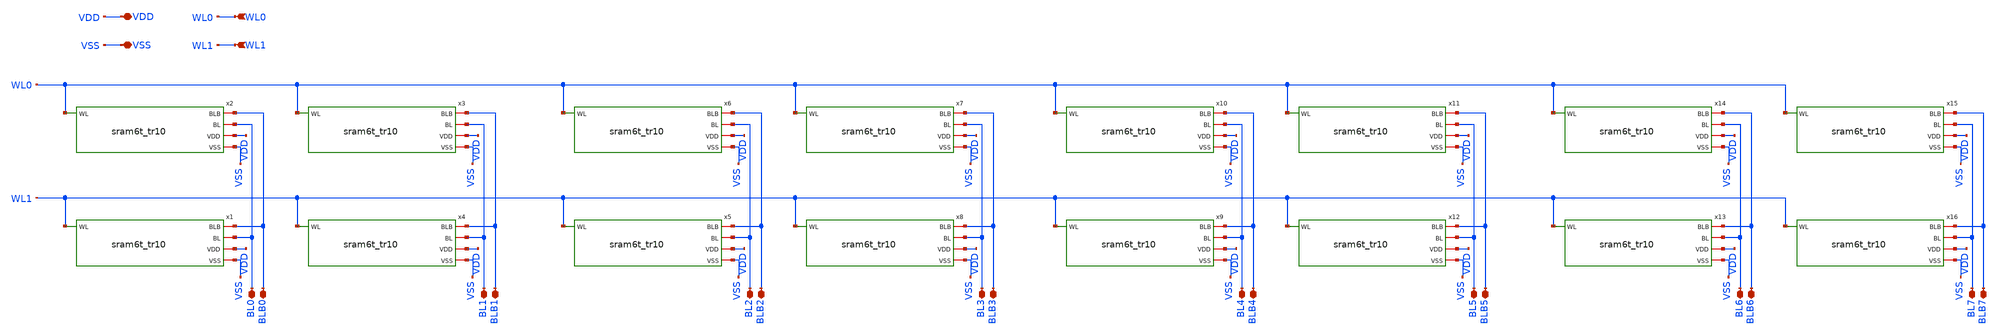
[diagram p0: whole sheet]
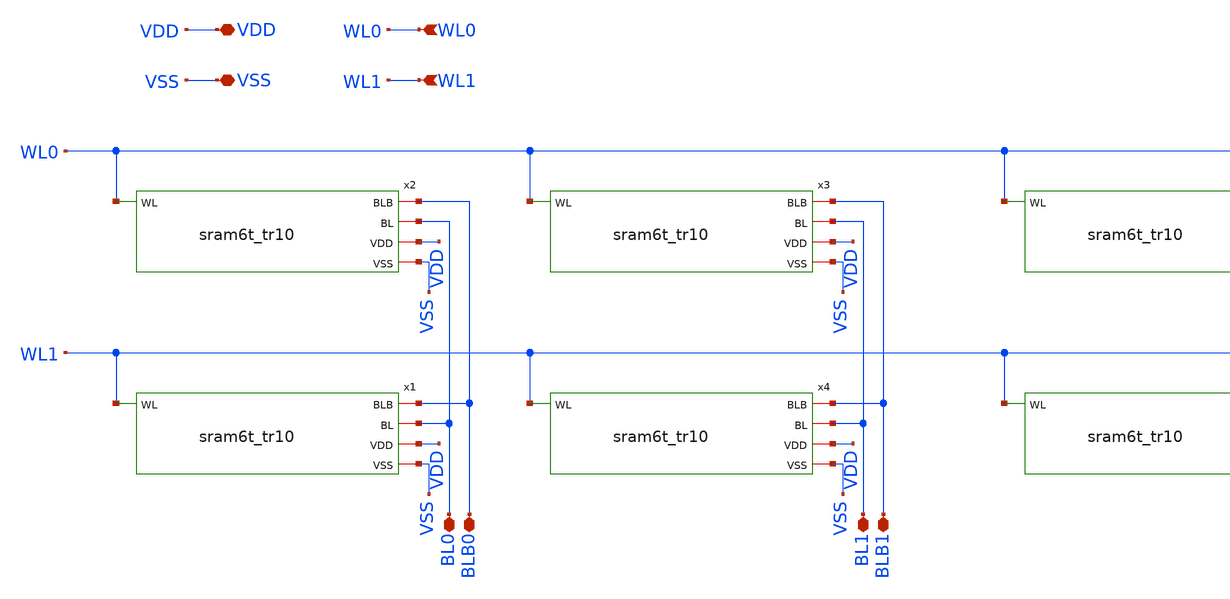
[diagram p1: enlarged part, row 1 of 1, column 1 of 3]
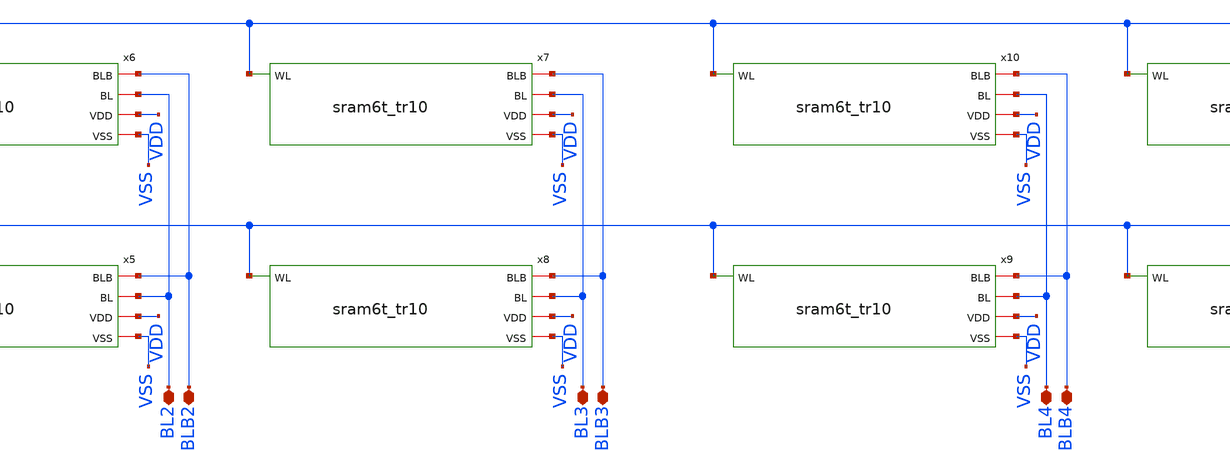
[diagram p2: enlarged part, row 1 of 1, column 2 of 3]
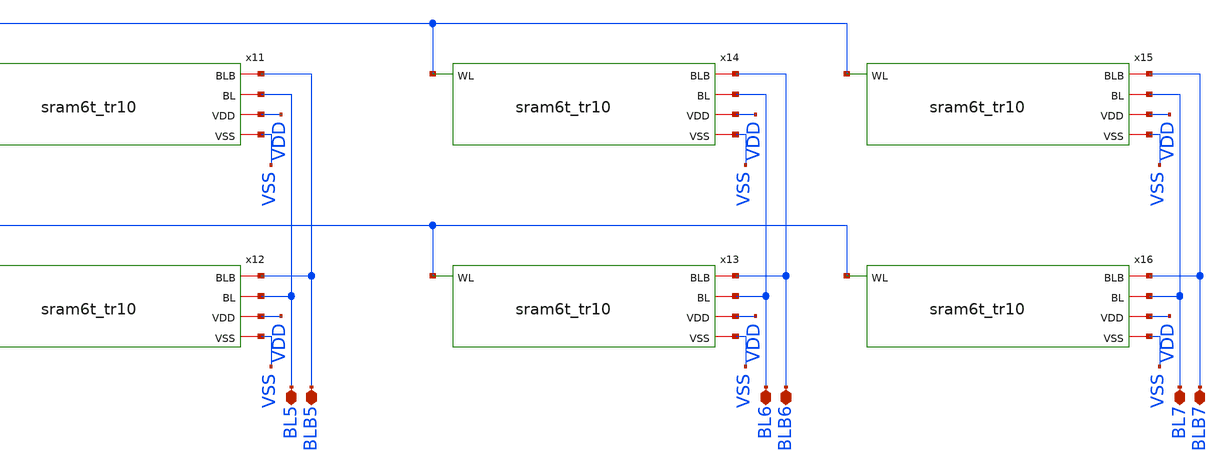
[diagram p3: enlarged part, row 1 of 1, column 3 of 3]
** sch_path: array/8word_x_2bit/sram_2w8b.sch
**.subckt sram_2w8b VDD VSS WL0 WL1 BL0 BLB0 BL1 BLB1 BL2 BLB2 BL3 BLB3 BL4 BLB4 BL5 BLB5 BL6 BLB6
*+ BL7 BLB7
*.iopin VDD
*.iopin VSS
*.ipin WL0
*.ipin WL1
*.iopin BL0
*.iopin BLB0
*.iopin BL1
*.iopin BLB1
*.iopin BL2
*.iopin BLB2
*.iopin BL3
*.iopin BLB3
*.iopin BL4
*.iopin BLB4
*.iopin BL5
*.iopin BLB5
*.iopin BL6
*.iopin BLB6
*.iopin BL7
*.iopin BLB7
x1 BL0 BLB0 WL1 VDD VSS sram6t_tr10
x2 BL0 BLB0 WL0 VDD VSS sram6t_tr10
x3 BL1 BLB1 WL0 VDD VSS sram6t_tr10
x4 BL1 BLB1 WL1 VDD VSS sram6t_tr10
x5 BL2 BLB2 WL1 VDD VSS sram6t_tr10
x6 BL2 BLB2 WL0 VDD VSS sram6t_tr10
x7 BL3 BLB3 WL0 VDD VSS sram6t_tr10
x8 BL3 BLB3 WL1 VDD VSS sram6t_tr10
x9 BL4 BLB4 WL1 VDD VSS sram6t_tr10
x10 BL4 BLB4 WL0 VDD VSS sram6t_tr10
x11 BL5 BLB5 WL0 VDD VSS sram6t_tr10
x12 BL5 BLB5 WL1 VDD VSS sram6t_tr10
x13 BL6 BLB6 WL1 VDD VSS sram6t_tr10
x14 BL6 BLB6 WL0 VDD VSS sram6t_tr10
x15 BL7 BLB7 WL0 VDD VSS sram6t_tr10
x16 BL7 BLB7 WL1 VDD VSS sram6t_tr10
**.ends
.end
